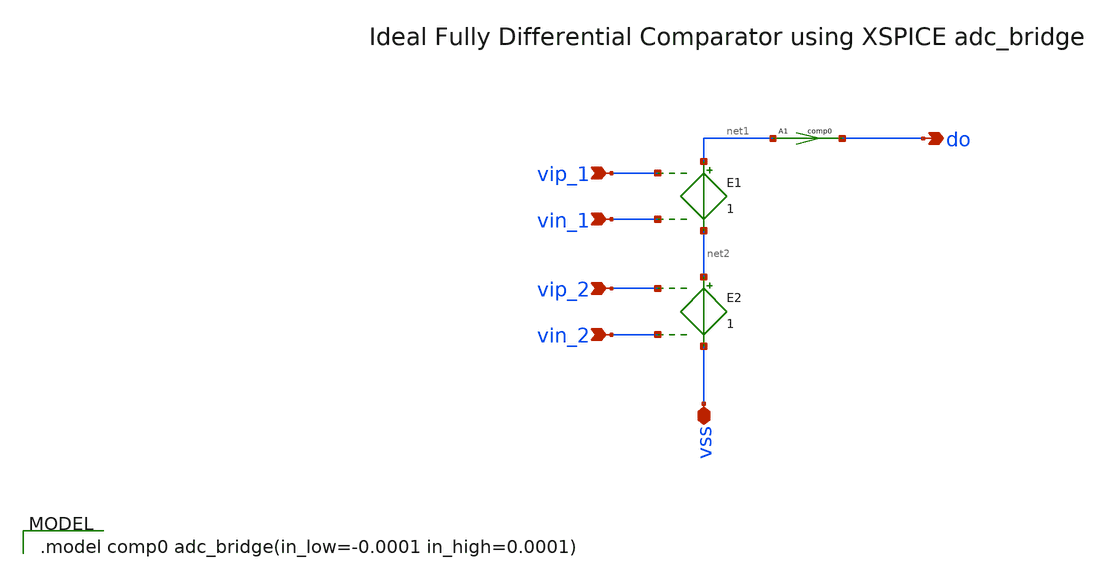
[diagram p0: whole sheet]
** sch_path: xschem/comp-macro.sch
**.subckt comp-macro vss vip_1 vin_1 vip_2 vin_2 do
*.iopin vss
*.ipin vip_1
*.ipin vin_1
*.ipin vip_2
*.ipin vin_2
*.opin do
A1 [ net1 ] [ do ] comp0
E1 net1 net2 vip_1 vin_1 1
E2 net2 vss vip_2 vin_2 1
**.ends
**** begin user architecture code

.model comp0 adc_bridge(in_low=-0.0001 in_high=0.0001)

**** end user architecture code
.end
